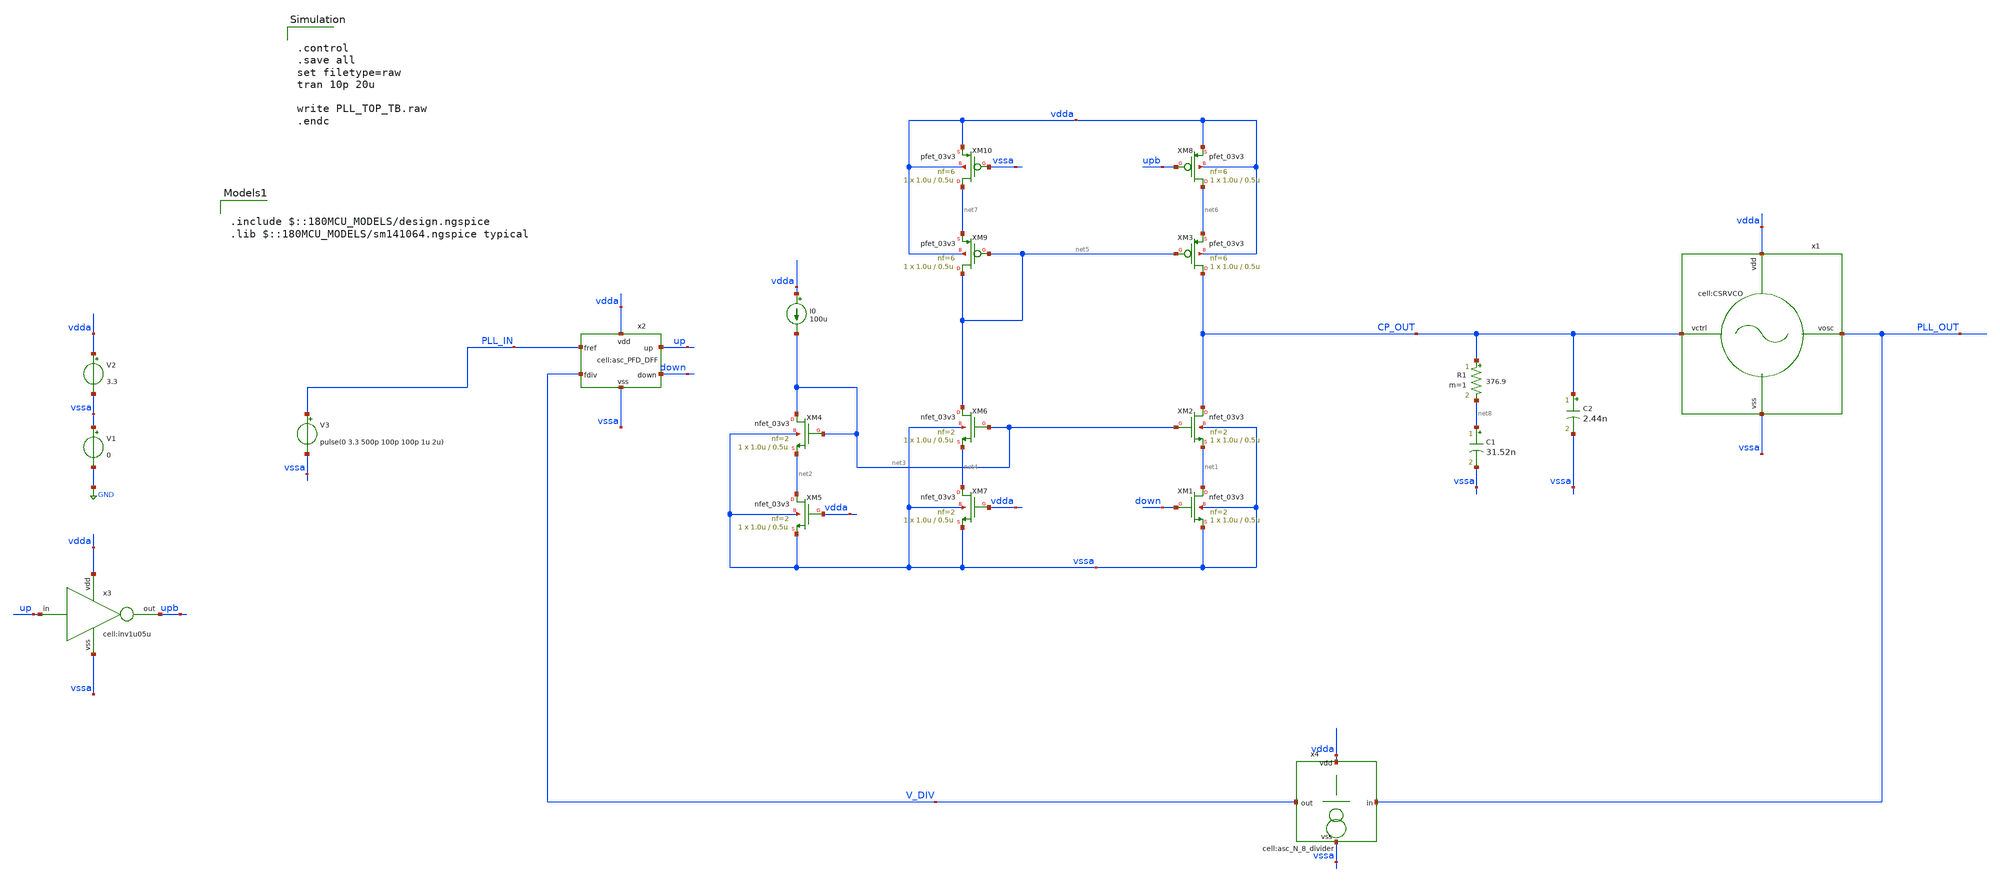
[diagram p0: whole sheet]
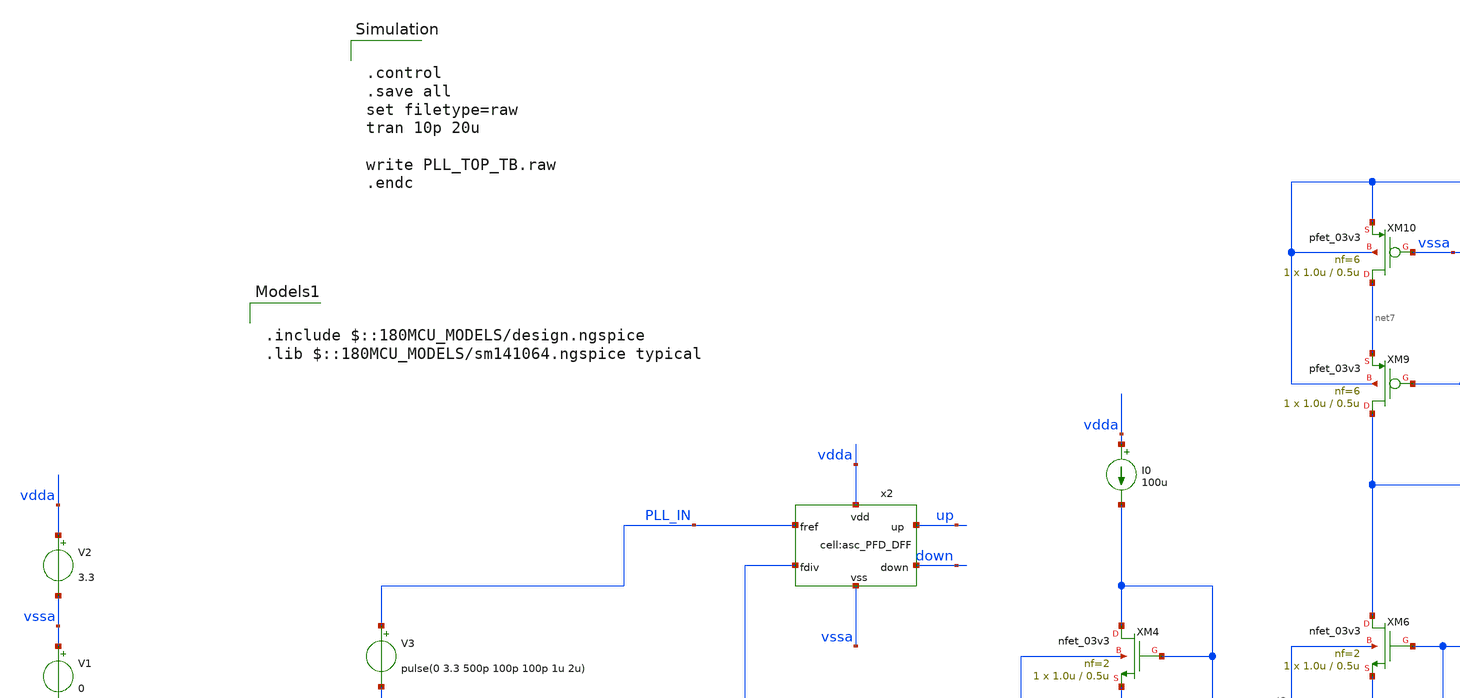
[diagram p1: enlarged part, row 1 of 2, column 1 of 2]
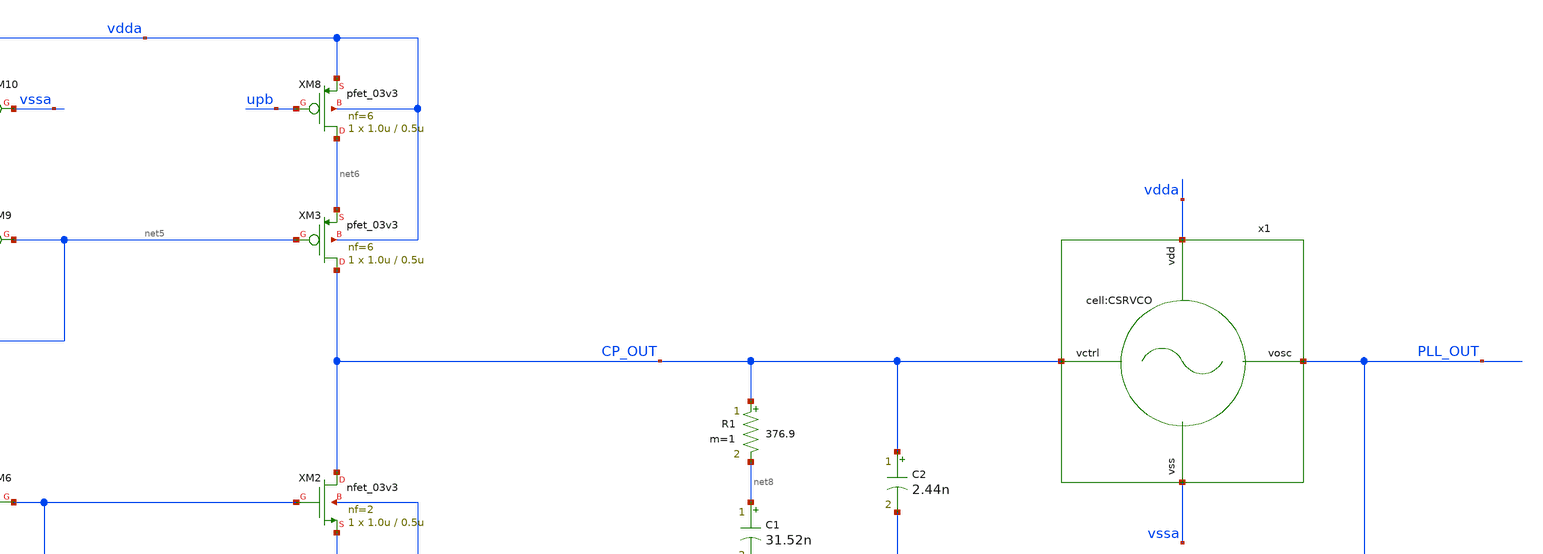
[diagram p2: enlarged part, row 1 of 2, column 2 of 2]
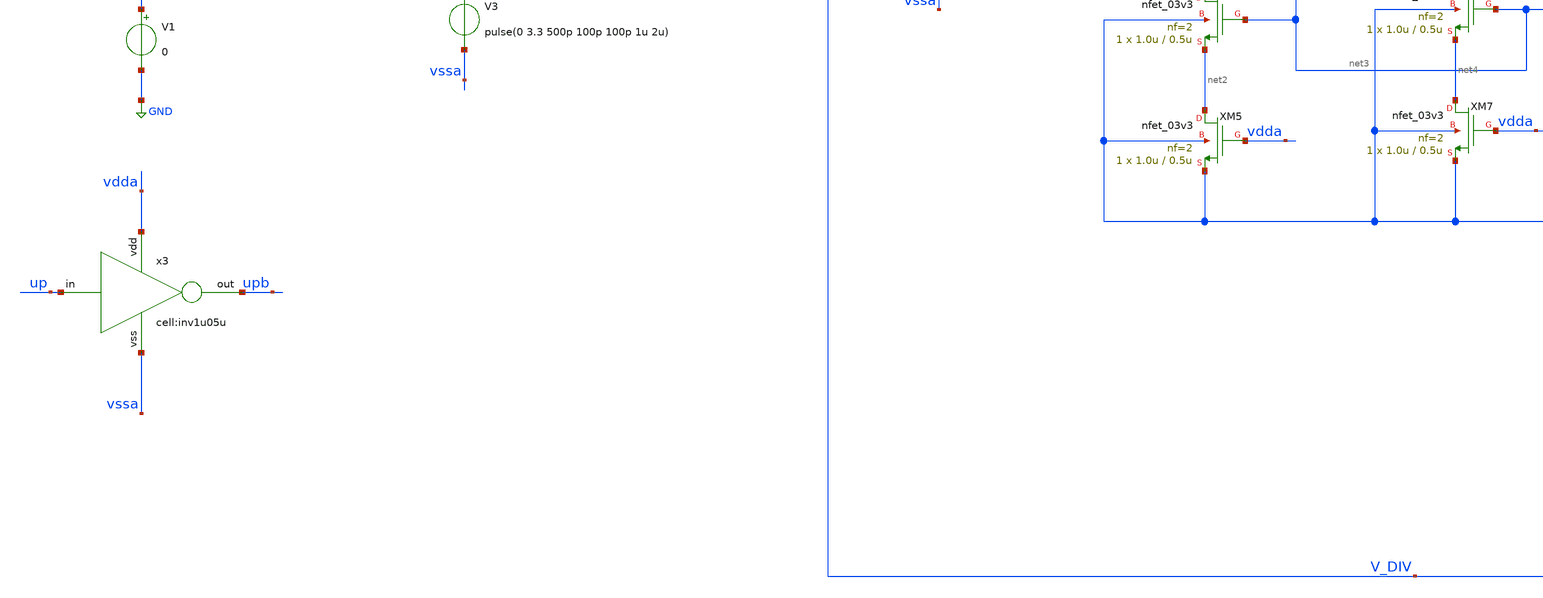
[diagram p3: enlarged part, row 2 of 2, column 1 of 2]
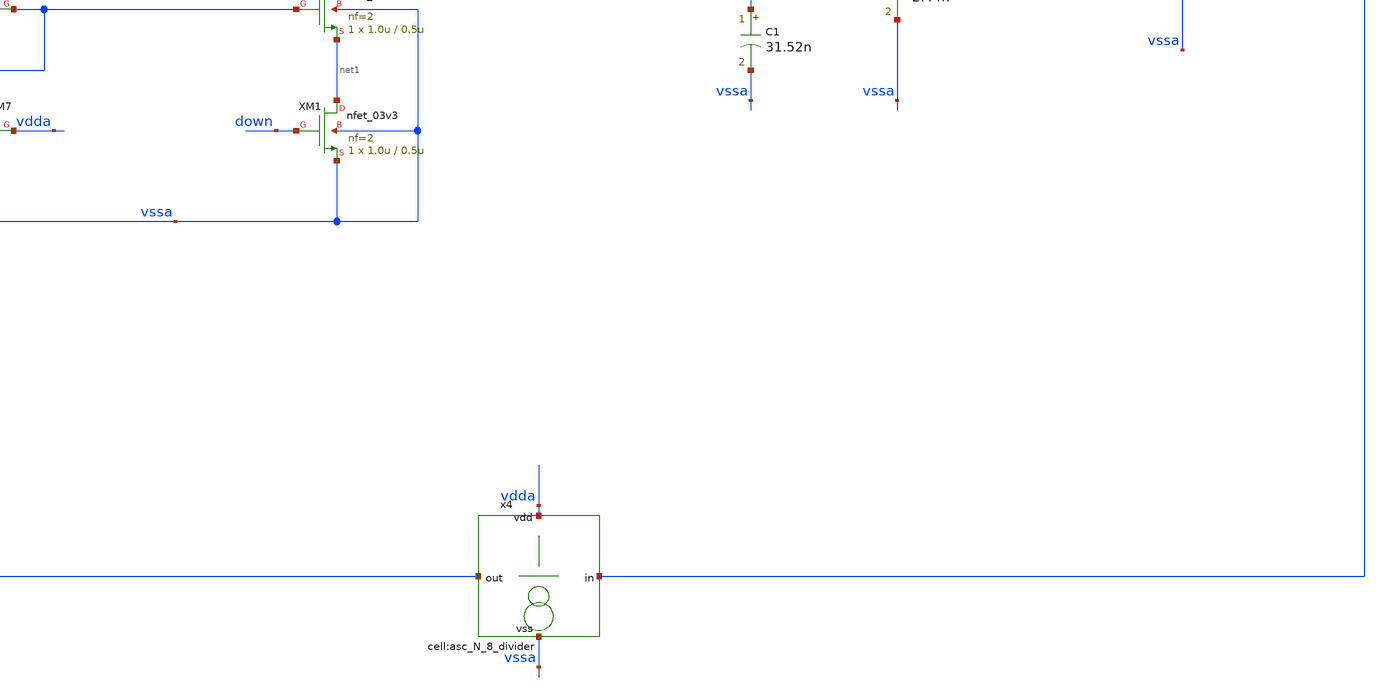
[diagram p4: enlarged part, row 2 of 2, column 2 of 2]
** sch_path: designs/libs/core_analog/PLL_TOP.sch
**.subckt PLL_TOP
x1 CP_OUT vdda vssa PLL_OUT CSRVCO
V1 vssa GND 0
V2 vdda vssa 3.3
x2 vdda vssa down up PLL_IN V_DIV asc_PFD_DFF
x3 up vdda upb vssa inv1u05u
XM2 CP_OUT net3 net1 vssa nfet_03v3 L=0.5u W=1.0u nf=2 ad='int((nf+1)/2) * W/nf * 0.18u' as='int((nf+2)/2) * W/nf * 0.18u'
+ pd='2*int((nf+1)/2) * (W/nf + 0.18u)' ps='2*int((nf+2)/2) * (W/nf + 0.18u)' nrd='0.18u / W' nrs='0.18u / W'
+ sa=0 sb=0 sd=0 m=1
XM3 CP_OUT net5 net6 vdda pfet_03v3 L=0.5u W=1.0u nf=6 ad='int((nf+1)/2) * W/nf * 0.18u' as='int((nf+2)/2) * W/nf * 0.18u'
+ pd='2*int((nf+1)/2) * (W/nf + 0.18u)' ps='2*int((nf+2)/2) * (W/nf + 0.18u)' nrd='0.18u / W' nrs='0.18u / W'
+ sa=0 sb=0 sd=0 m=1
XM1 net1 down vssa vssa nfet_03v3 L=0.5u W=1.0u nf=2 ad='int((nf+1)/2) * W/nf * 0.18u' as='int((nf+2)/2) * W/nf * 0.18u'
+ pd='2*int((nf+1)/2) * (W/nf + 0.18u)' ps='2*int((nf+2)/2) * (W/nf + 0.18u)' nrd='0.18u / W' nrs='0.18u / W'
+ sa=0 sb=0 sd=0 m=1
XM4 net3 net3 net2 vssa nfet_03v3 L=0.5u W=1.0u nf=2 ad='int((nf+1)/2) * W/nf * 0.18u' as='int((nf+2)/2) * W/nf * 0.18u'
+ pd='2*int((nf+1)/2) * (W/nf + 0.18u)' ps='2*int((nf+2)/2) * (W/nf + 0.18u)' nrd='0.18u / W' nrs='0.18u / W'
+ sa=0 sb=0 sd=0 m=1
XM5 net2 vdda vssa vssa nfet_03v3 L=0.5u W=1.0u nf=2 ad='int((nf+1)/2) * W/nf * 0.18u' as='int((nf+2)/2) * W/nf * 0.18u'
+ pd='2*int((nf+1)/2) * (W/nf + 0.18u)' ps='2*int((nf+2)/2) * (W/nf + 0.18u)' nrd='0.18u / W' nrs='0.18u / W'
+ sa=0 sb=0 sd=0 m=1
XM6 net5 net3 net4 vssa nfet_03v3 L=0.5u W=1.0u nf=2 ad='int((nf+1)/2) * W/nf * 0.18u' as='int((nf+2)/2) * W/nf * 0.18u'
+ pd='2*int((nf+1)/2) * (W/nf + 0.18u)' ps='2*int((nf+2)/2) * (W/nf + 0.18u)' nrd='0.18u / W' nrs='0.18u / W'
+ sa=0 sb=0 sd=0 m=1
XM7 net4 vdda vssa vssa nfet_03v3 L=0.5u W=1.0u nf=2 ad='int((nf+1)/2) * W/nf * 0.18u' as='int((nf+2)/2) * W/nf * 0.18u'
+ pd='2*int((nf+1)/2) * (W/nf + 0.18u)' ps='2*int((nf+2)/2) * (W/nf + 0.18u)' nrd='0.18u / W' nrs='0.18u / W'
+ sa=0 sb=0 sd=0 m=1
XM8 net6 upb vdda vdda pfet_03v3 L=0.5u W=1.0u nf=6 ad='int((nf+1)/2) * W/nf * 0.18u' as='int((nf+2)/2) * W/nf * 0.18u'
+ pd='2*int((nf+1)/2) * (W/nf + 0.18u)' ps='2*int((nf+2)/2) * (W/nf + 0.18u)' nrd='0.18u / W' nrs='0.18u / W'
+ sa=0 sb=0 sd=0 m=1
XM9 net5 net5 net7 vdda pfet_03v3 L=0.5u W=1.0u nf=6 ad='int((nf+1)/2) * W/nf * 0.18u' as='int((nf+2)/2) * W/nf * 0.18u'
+ pd='2*int((nf+1)/2) * (W/nf + 0.18u)' ps='2*int((nf+2)/2) * (W/nf + 0.18u)' nrd='0.18u / W' nrs='0.18u / W'
+ sa=0 sb=0 sd=0 m=1
XM10 net7 vssa vdda vdda pfet_03v3 L=0.5u W=1.0u nf=6 ad='int((nf+1)/2) * W/nf * 0.18u' as='int((nf+2)/2) * W/nf * 0.18u'
+ pd='2*int((nf+1)/2) * (W/nf + 0.18u)' ps='2*int((nf+2)/2) * (W/nf + 0.18u)' nrd='0.18u / W' nrs='0.18u / W'
+ sa=0 sb=0 sd=0 m=1
I0 vdda net3 100u
C1 net8 vssa 31.52n m=1
R1 CP_OUT net8 376.9 m=1
C2 CP_OUT vssa 2.44n m=1
x4 PLL_OUT V_DIV vdda vssa asc_N_8_divider
V3 PLL_IN vssa pulse(0 3.3 500p 100p 100p 1u 2u)
**** begin user architecture code

.include $::180MCU_MODELS/design.ngspice
.lib $::180MCU_MODELS/sm141064.ngspice typical



.control
.save all
set filetype=raw
tran 10p 20u

write PLL_TOP_TB.raw
.endc


**** end user architecture code
**.ends
.GLOBAL GND
.end
